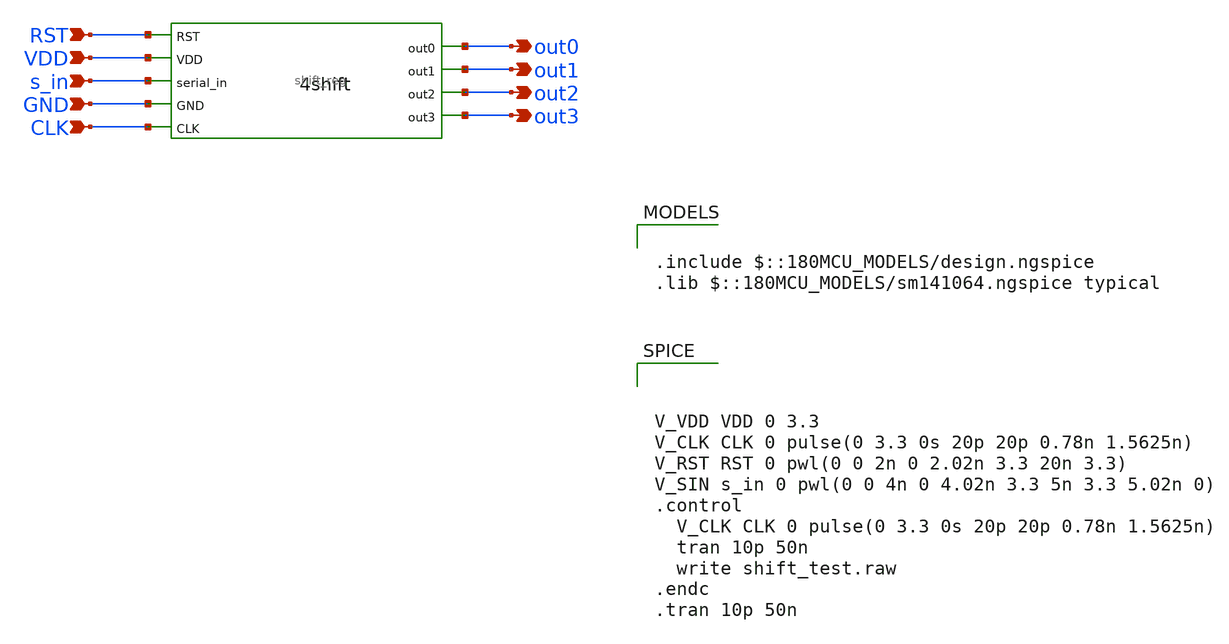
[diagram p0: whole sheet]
** sch_path: blocks/dsp-fft/tb/shift_reg_tb.sch
**.subckt shift_reg_tb VDD RST GND CLK out0 out1 out2 out3 s_in
*.ipin VDD
*.ipin RST
*.ipin GND
*.ipin CLK
*.opin out0
*.opin out1
*.opin out2
*.opin out3
*.ipin s_in
x1 out1 out2 out3 out0 RST VDD s_in GND CLK shift_reg
**** begin user architecture code

.include $::180MCU_MODELS/design.ngspice
.lib $::180MCU_MODELS/sm141064.ngspice typical




V_VDD VDD 0 3.3
V_CLK CLK 0 pulse(0 3.3 0s 20p 20p 0.78n 1.5625n)
V_RST RST 0 pwl(0 0 2n 0 2.02n 3.3 20n 3.3)
V_SIN s_in 0 pwl(0 0 4n 0 4.02n 3.3 5n 3.3 5.02n 0)
.control
  V_CLK CLK 0 pulse(0 3.3 0s 20p 20p 0.78n 1.5625n)
  tran 10p 50n
  write shift_test.raw
.endc
.tran 10p 50n



**** end user architecture code
**.ends
.end
